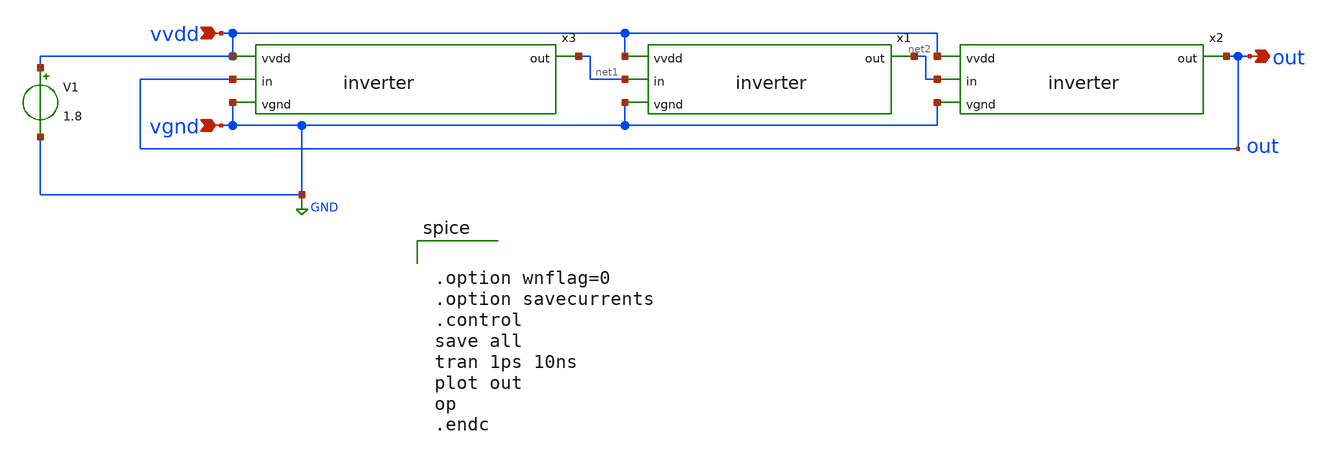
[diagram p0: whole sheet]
** sch_path: ring_oscillator/tb_ring_oscillator.sch
**.subckt tb_ring_oscillator vvdd vgnd out
*.ipin vvdd
*.ipin vgnd
*.opin out
x1 vvdd net1 net2 vgnd inverter
x2 vvdd net2 out vgnd inverter
x3 vvdd out net1 vgnd inverter
V1 vvdd vgnd 1.8
**** begin user architecture code

** opencircuitdesign pdks install
.lib $::SKYWATER_MODELS/sky130.lib.spice tt



.option wnflag=0
.option savecurrents
.control
save all
tran 1ps 10ns
plot out
op
.endc


**** end user architecture code
**.ends
.GLOBAL GND
.end
